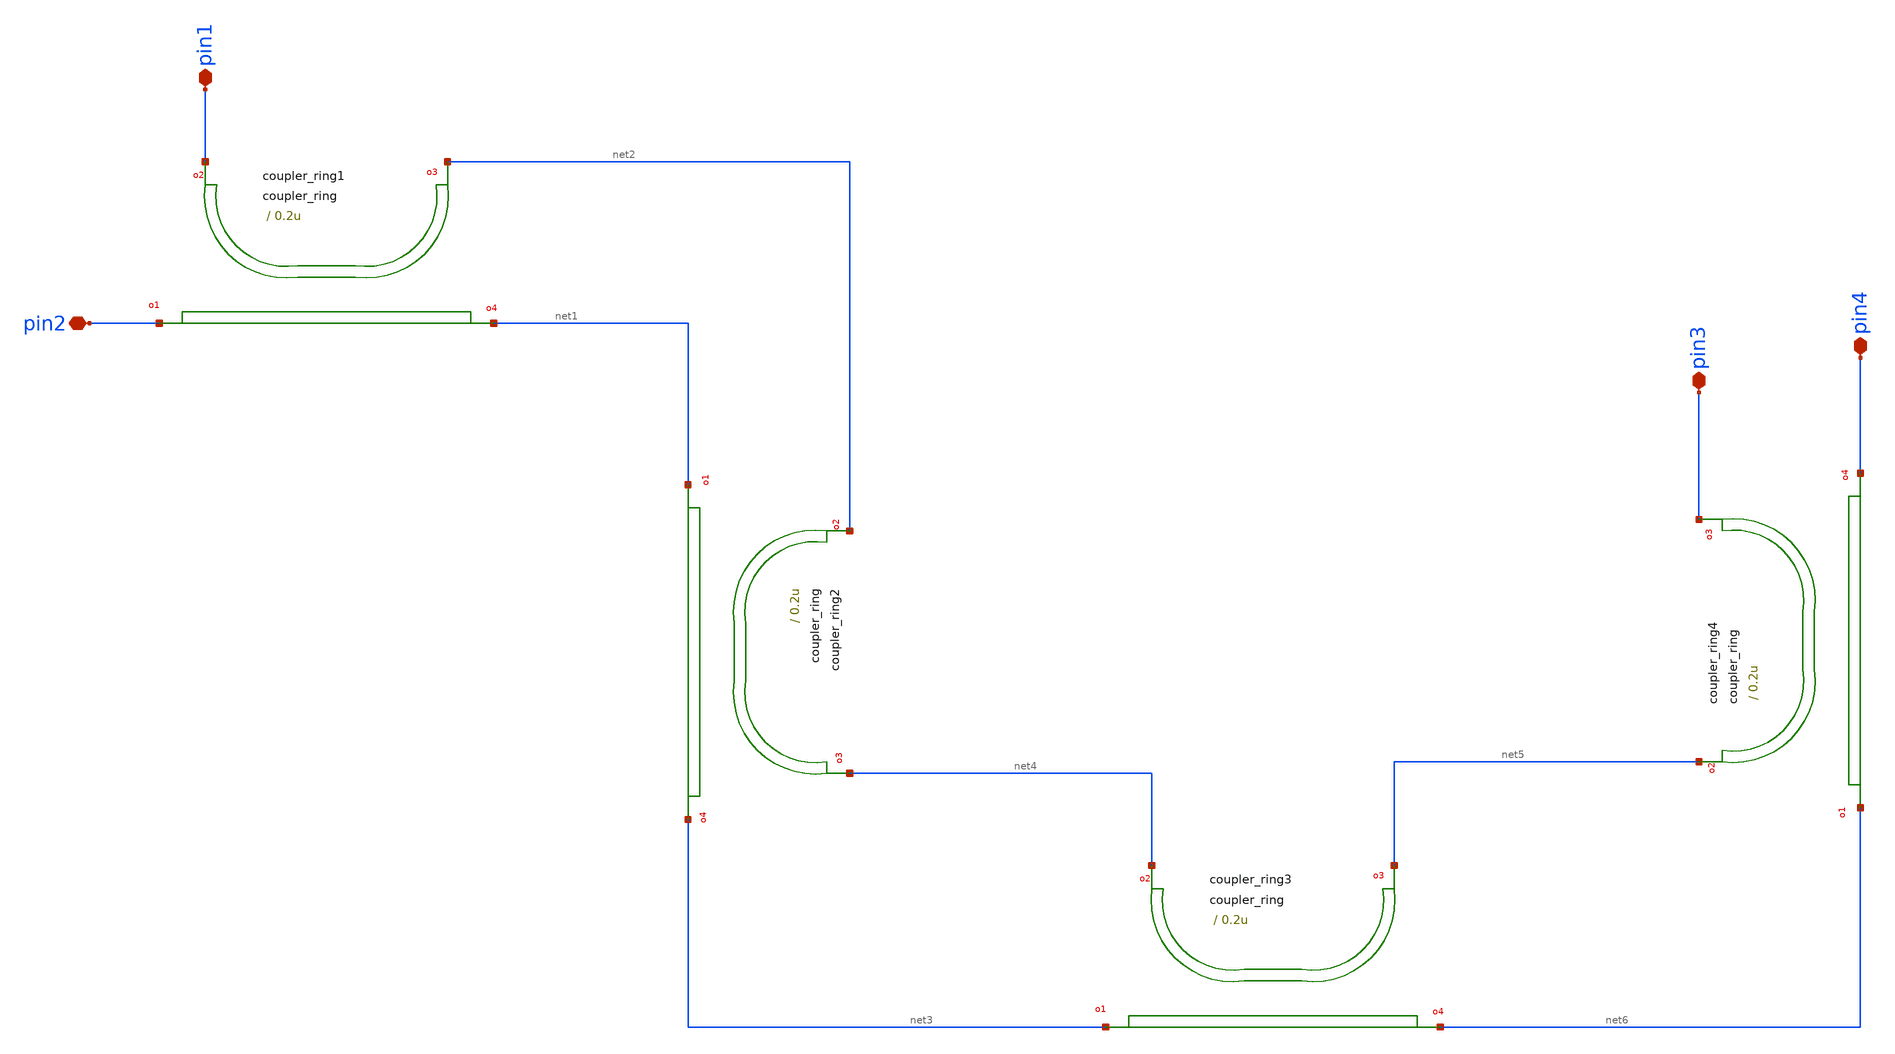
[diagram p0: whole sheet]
** sch_path: xschem/tests/test_sch/test_coupler_ring.sch
* Copyright (c) 2024, Mabrains LLC
* Licensed under the GNU Lesser General Public License, Version 3.0 (the "License");
* you may not use this file except in compliance with the License.
* GNU Lesser General Public License
* Version 3, 29 June 2007
* This program is free software: you can redistribute it and/or modify
* it under the terms of the GNU Lesser General Public License as published
* by the Free Software Foundation, either version 3 of the License, or
* (at your option) any later version.
* This program is distributed in the hope that it will be useful,
* but WITHOUT ANY WARRANTY; without even the implied warranty of
* MERCHANTABILITY or FITNESS FOR A PARTICULAR PURPOSE.  See the
* GNU Lesser General Public License for more details.
* You should have received a copy of the GNU Lesser General Public License
* along with this program.  If not, see <https://www.gnu.org/licenses/>.
* SPDX-License-Identifier: LGPL-3.0
**.subckt test_coupler_ring pin2 pin1 pin3 pin4
*.iopin pin2
*.iopin pin1
*.iopin pin3
*.iopin pin4
Pcoupler_ring1 pin2 net1 net2 pin1 coupler_ring gap=0.2u radius=5.0u length_x=4.0u
+ length_extension=3.0u
Pcoupler_ring3 net3 net6 net5 net4 coupler_ring gap=0.2u radius=5.0u length_x=4.0u
+ length_extension=3.0u
Pcoupler_ring4 net6 pin4 pin3 net5 coupler_ring gap=0.2u radius=5.0u length_x=4.0u
+ length_extension=3.0u
Pcoupler_ring2 net1 net3 net4 net2 coupler_ring gap=0.2u radius=5.0u length_x=4.0u
+ length_extension=3.0u
**.ends
.end
